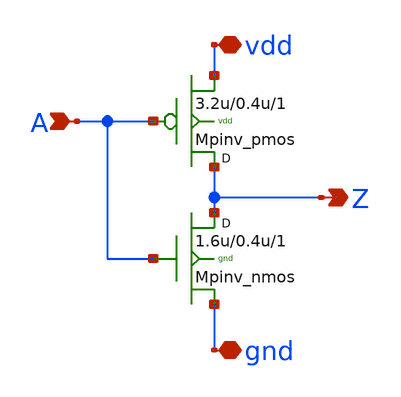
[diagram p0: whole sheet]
** sch_path: sram_2_16_scn4m/pinv_10.sch
**.subckt pinv_10 A Z vdd gnd
*.ipin A
*.opin Z
*.iopin vdd
*.iopin gnd
Mpinv_nmos Z A gnd gnd n w=1.6u l=0.4u m=1
Mpinv_pmos Z A vdd vdd p w=3.2u l=0.4u m=1
**.ends
.end
